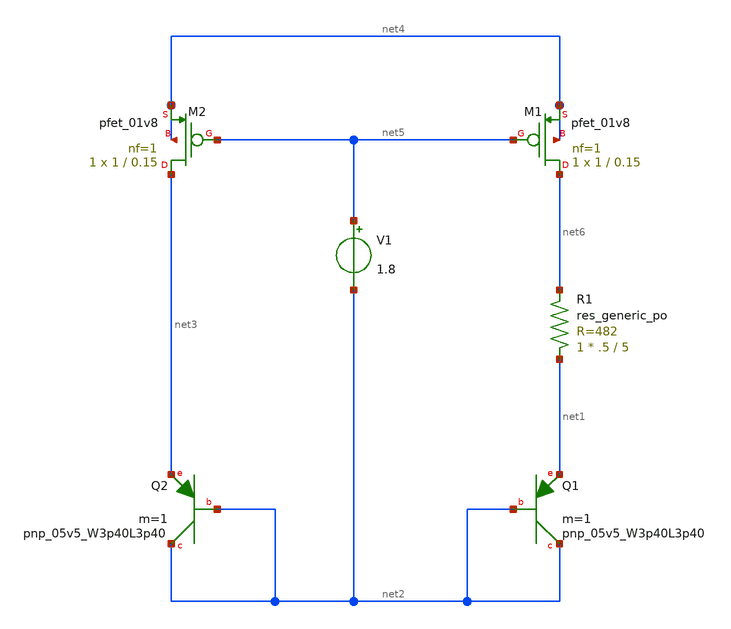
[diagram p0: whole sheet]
** sch_path: design/CNR_GR02_SKY130NM/bi_CM.sch
**.subckt bi_CM
XQ1 net2 net2 net1 sky130_fd_pr__pnp_05v5_W3p40L3p40 m=1
XR1 net1 net6 sky130_fd_pr__res_generic_po W=.5 L=5 m=1
XM1 net6 net5 net4 net4 sky130_fd_pr__pfet_01v8 L=0.15 W=1 nf=1 ad='int((nf+1)/2) * W/nf * 0.29' as='int((nf+2)/2) * W/nf * 0.29'
+ pd='2*int((nf+1)/2) * (W/nf + 0.29)' ps='2*int((nf+2)/2) * (W/nf + 0.29)' nrd='0.29 / W' nrs='0.29 / W'
+ sa=0 sb=0 sd=0 mult=1 m=1
XM2 net3 net5 net4 net4 sky130_fd_pr__pfet_01v8 L=0.15 W=1 nf=1 ad='int((nf+1)/2) * W/nf * 0.29' as='int((nf+2)/2) * W/nf * 0.29'
+ pd='2*int((nf+1)/2) * (W/nf + 0.29)' ps='2*int((nf+2)/2) * (W/nf + 0.29)' nrd='0.29 / W' nrs='0.29 / W'
+ sa=0 sb=0 sd=0 mult=1 m=1
XQ2 net2 net2 net3 sky130_fd_pr__pnp_05v5_W3p40L3p40 m=1
V1 net5 net2 1.8
**.ends
.end
